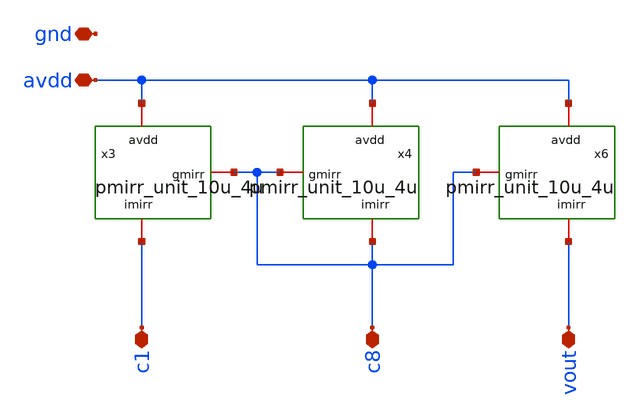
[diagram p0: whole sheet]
** sch_path: xschem/rev_1/pmirr_10u_4u.sch
**.subckt pmirr_10u_4u c8 c1 vout avdd gnd
*.iopin c8
*.iopin c1
*.iopin vout
*.iopin avdd
*.iopin gnd
x3 avdd c8 c1 pmirr_unit_10u_4u
x4 avdd c8 c8 pmirr_unit_10u_4u
x6 avdd c8 vout pmirr_unit_10u_4u
**.ends
.end
